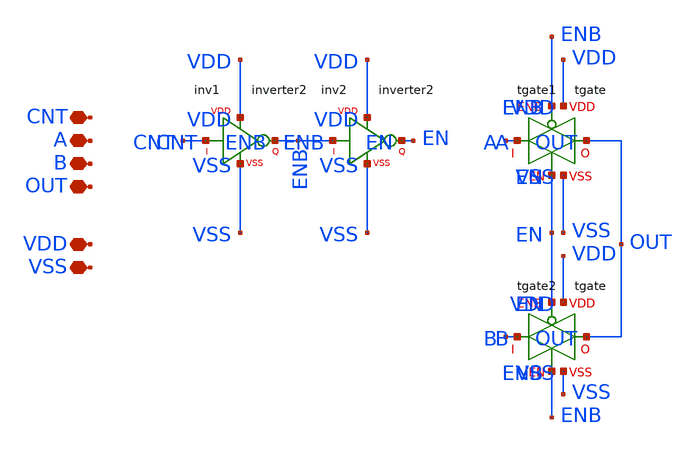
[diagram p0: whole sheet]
** sch_path: xschem/mux_2to1_generated_sky130_fd_pr/mux_2to1/analogMux_wrapper.sch
**.subckt analogMux_wrapper CNT A B OUT VDD VSS
*.iopin CNT
*.iopin A
*.iopin B
*.iopin OUT
*.iopin VDD
*.iopin VSS
Xinv1 VDD VSS CNT ENB inverter2
Xinv2 VDD VSS ENB EN inverter2
Xtgate1 ENB EN VDD VSS A OUT tgate
Xtgate2 EN ENB VDD VSS B OUT tgate
**.ends

* expanding   symbol:  mux_2to1_generated_sky130_fd_pr/inverter2/inverter2.sym # of pins=4
** sym_path: xschem/mux_2to1_generated_sky130_fd_pr/inverter2/inverter2.sym
** sch_path: xschem/mux_2to1_generated_sky130_fd_pr/inverter2/inverter2.sch
.subckt inverter2 VDD VSS in out


*.iopin VDD
*.iopin VSS
*.ipin in
*.opin out
XMN out in VSS VSS nmos4_lvt w=1.5 l=0.45 nf=20
XMP out in VDD VDD pmos4_lvt w=1.5 l=0.45 nf=40
XMDUMMY0 VSS VSS VSS VSS nmos4_lvt w=1.5 l=0.45 nf=124
XMDUMMY1 VDD VDD VDD VDD pmos4_lvt w=1.5 l=0.45 nf=104
.ends


* expanding   symbol:  mux_2to1_generated_sky130_fd_pr/tgate/tgate.sym # of pins=6
** sym_path: xschem/mux_2to1_generated_sky130_fd_pr/tgate/tgate.sym
** sch_path: xschem/mux_2to1_generated_sky130_fd_pr/tgate/tgate.sch
.subckt tgate ENB EN VDD VSS I O


*.ipin EN
*.ipin ENB
*.iopin I
*.iopin O
*.iopin VDD
*.iopin VSS
XMN0 O EN I VSS nmos4_lvt w=1.5 l=0.45 nf=30
XMP0 O ENB I VDD pmos4_lvt w=1.5 l=0.45 nf=90
XMDUMMY0 VSS VSS VSS VSS nmos4_lvt w=1.5 l=0.45 nf=262
XMDUMMY1 I VSS VSS VSS nmos4_lvt w=1.5 l=0.45 nf=2
XMDUMMY2 VDD VDD VDD VDD pmos4_lvt w=1.5 l=0.45 nf=202
XMDUMMY3 I VDD VDD VDD pmos4_lvt w=1.5 l=0.45 nf=2
.ends


* expanding   symbol:  mux_2to1_generated_sky130_fd_pr/BAG_prim/nmos4_lvt/nmos4_lvt.sym # of pins=4
** sym_path: xschem/mux_2to1_generated_sky130_fd_pr/BAG_prim/nmos4_lvt/nmos4_lvt.sym
** sch_path: xschem/mux_2to1_generated_sky130_fd_pr/BAG_prim/nmos4_lvt/nmos4_lvt.sch
.subckt nmos4_lvt D G S B model
w=100n
l=18n
nf=4
model=nmos4_lvt


*.iopin D
*.iopin G
*.iopin S
*.iopin B
MM1 D G S B sky130_fd_pr__nfet_01v8_lvt L=l W='w * nf ' nf=nf ad='int((nf+1)/2) * W * 0.29u' as='int((nf+2)/2) * W * 0.29u'
+ pd='2*int((nf+1)/2) * (W + 0.29u)' ps='2*int((nf+2)/2) * (W + 0.29u)' nrd='0.29u*nf / W' nrs='0.29u*nf / W'
+ sa=0 sb=0 sd=0 mult=1 m=1
.ends


* expanding   symbol:  mux_2to1_generated_sky130_fd_pr/BAG_prim/pmos4_lvt/pmos4_lvt.sym # of pins=4
** sym_path: xschem/mux_2to1_generated_sky130_fd_pr/BAG_prim/pmos4_lvt/pmos4_lvt.sym
** sch_path: xschem/mux_2to1_generated_sky130_fd_pr/BAG_prim/pmos4_lvt/pmos4_lvt.sch
.subckt pmos4_lvt D G S B model
w=100n
l=18n
nf=4
model=pmos4_lvt


*.iopin D
*.iopin G
*.iopin S
*.iopin B
MM1 D G S B sky130_fd_pr__pfet_01v8_lvt L=l W='w * nf ' nf=nf ad='int((nf+1)/2) * W * 0.29u' as='int((nf+2)/2) * W * 0.29u'
+ pd='2*int((nf+1)/2) * (W + 0.29u)' ps='2*int((nf+2)/2) * (W + 0.29u)' nrd='0.29u*nf / W' nrs='0.29u*nf / W'
+ sa=0 sb=0 sd=0 mult=1 m=1
.ends

.end
